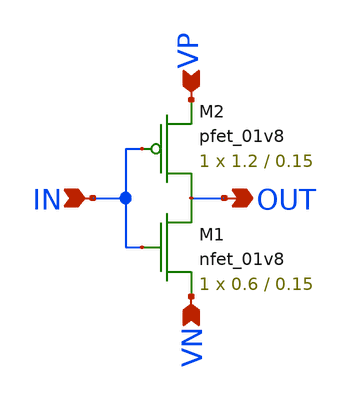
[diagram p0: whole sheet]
** sch_path: Mixed-Signal TRNG/xschem/inv_tap.sch
**.subckt inv_tap IN OUT VP VN
*.ipin IN
*.opin OUT
*.ipin VP
*.ipin VN
XM1 OUT IN VN VN sky130_fd_pr__nfet_01v8 L=0.15 W=0.6 nf=1 ad='int((nf+1)/2) * W/nf * 0.29' as='int((nf+2)/2) * W/nf * 0.29'
+ pd='2*int((nf+1)/2) * (W/nf + 0.29)' ps='2*int((nf+2)/2) * (W/nf + 0.29)' nrd='0.29 / W' nrs='0.29 / W'
+ sa=0 sb=0 sd=0 mult=1 m=1
XM2 OUT IN VP VP sky130_fd_pr__pfet_01v8 L=0.15 W=1.2 nf=1 ad='int((nf+1)/2) * W/nf * 0.29' as='int((nf+2)/2) * W/nf * 0.29'
+ pd='2*int((nf+1)/2) * (W/nf + 0.29)' ps='2*int((nf+2)/2) * (W/nf + 0.29)' nrd='0.29 / W' nrs='0.29 / W'
+ sa=0 sb=0 sd=0 mult=1 m=1
**.ends
.end
